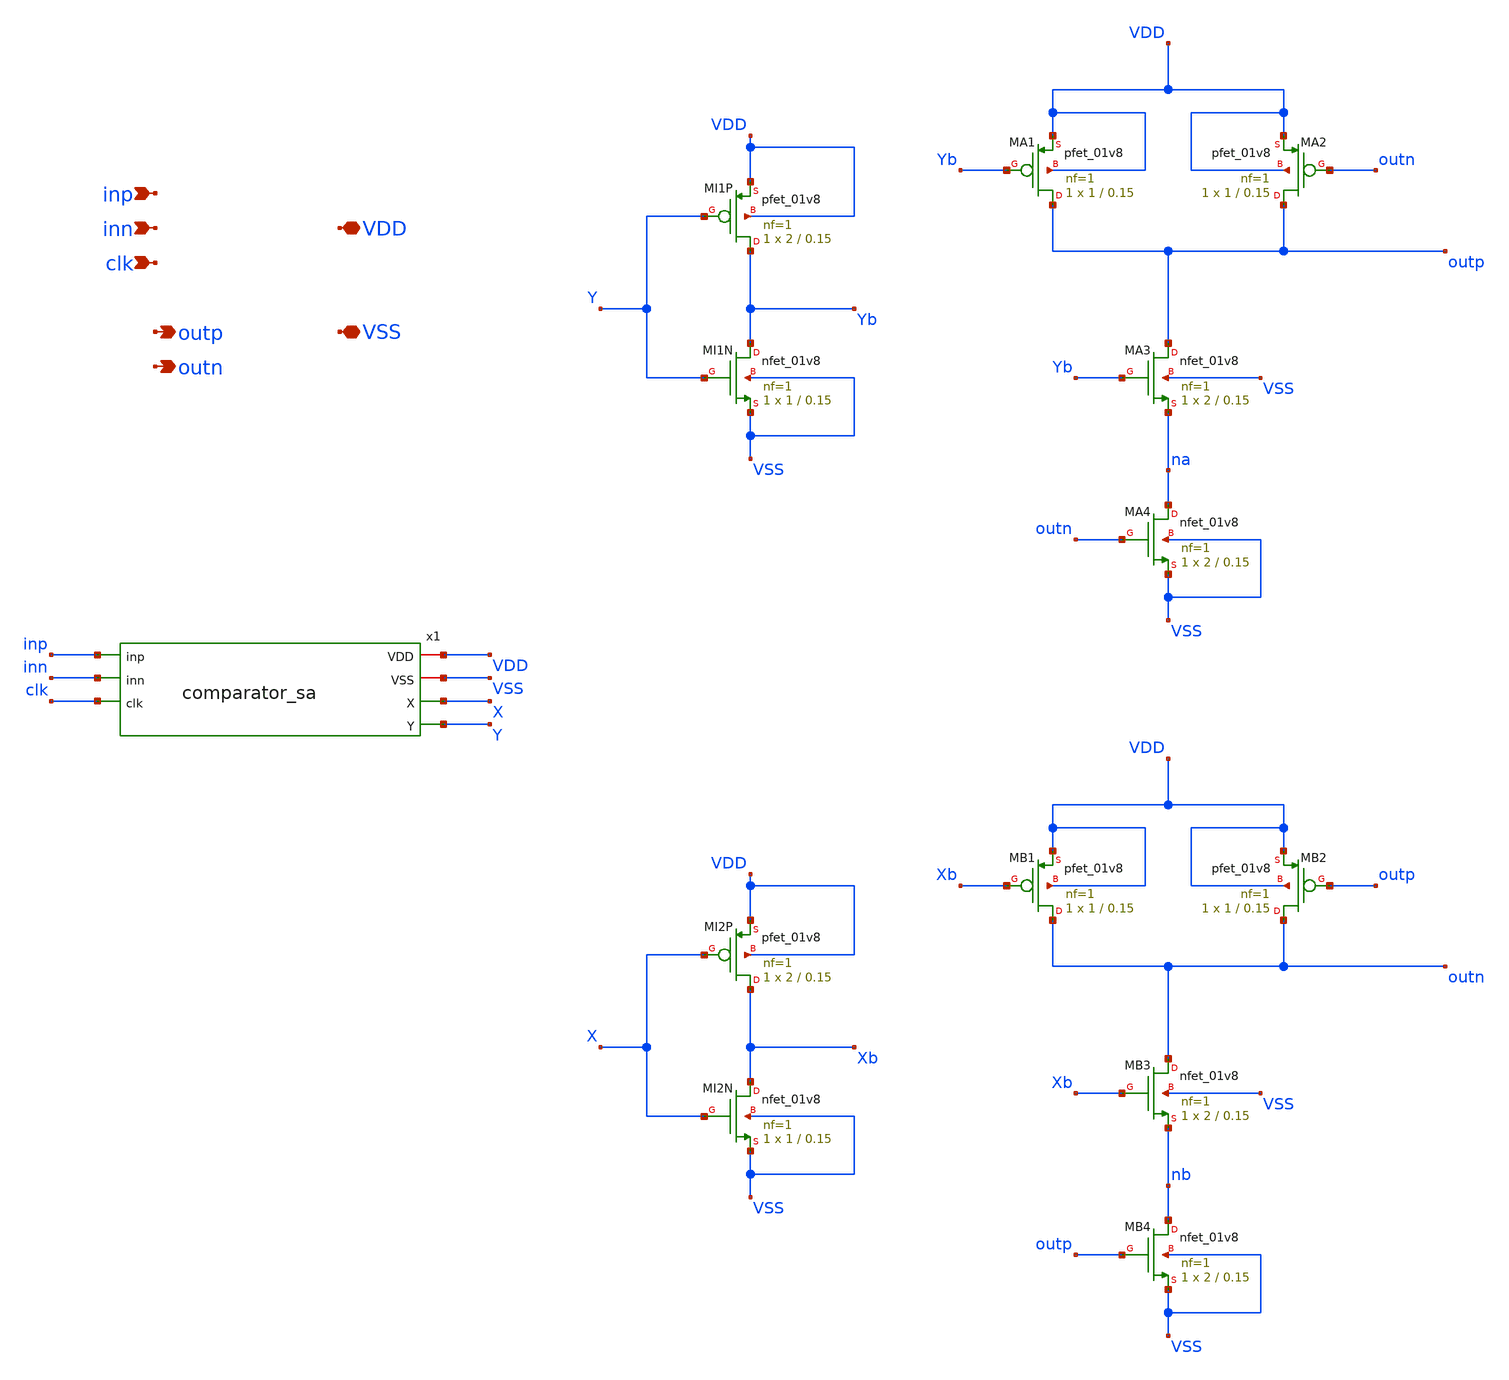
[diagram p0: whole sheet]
** sch_path: xschem/comparator.sch
**.subckt comparator inp inn clk outp outn VDD VSS
*.ipin inp
*.ipin inn
*.ipin clk
*.opin outp
*.opin outn
*.iopin VDD
*.iopin VSS
x1 inp VDD inn clk VSS X Y comparator_sa
XMI1N Yb Y VSS VSS sky130_fd_pr__nfet_01v8 L=0.15 W=1 nf=1 ad='int((1 + 1)/2) * 1 / 1 * 0.29' as='int((1 + 2)/2) * 1 / 1 * 0.29'
+ pd='2*int((1 + 1)/2) * (1 / 1 + 0.29)' ps='2*int((1 + 2)/2) * (1 / 1 + 0.29)' nrd='0.29 / 1 ' nrs='0.29 / 1 '
+ sa=0 sb=0 sd=0 mult=1 m=1
XMI1P Yb Y VDD VDD sky130_fd_pr__pfet_01v8 L=0.15 W=2 nf=1 ad='int((1 + 1)/2) * 2 / 1 * 0.29' as='int((1 + 2)/2) * 2 / 1 * 0.29'
+ pd='2*int((1 + 1)/2) * (2 / 1 + 0.29)' ps='2*int((1 + 2)/2) * (2 / 1 + 0.29)' nrd='0.29 / 2 ' nrs='0.29 / 2 '
+ sa=0 sb=0 sd=0 mult=1 m=1
XMI2N Xb X VSS VSS sky130_fd_pr__nfet_01v8 L=0.15 W=1 nf=1 ad='int((1 + 1)/2) * 1 / 1 * 0.29' as='int((1 + 2)/2) * 1 / 1 * 0.29'
+ pd='2*int((1 + 1)/2) * (1 / 1 + 0.29)' ps='2*int((1 + 2)/2) * (1 / 1 + 0.29)' nrd='0.29 / 1 ' nrs='0.29 / 1 '
+ sa=0 sb=0 sd=0 mult=1 m=1
XMI2P Xb X VDD VDD sky130_fd_pr__pfet_01v8 L=0.15 W=2 nf=1 ad='int((1 + 1)/2) * 2 / 1 * 0.29' as='int((1 + 2)/2) * 2 / 1 * 0.29'
+ pd='2*int((1 + 1)/2) * (2 / 1 + 0.29)' ps='2*int((1 + 2)/2) * (2 / 1 + 0.29)' nrd='0.29 / 2 ' nrs='0.29 / 2 '
+ sa=0 sb=0 sd=0 mult=1 m=1
XMA1 outp Yb VDD VDD sky130_fd_pr__pfet_01v8 L=0.15 W=1 nf=1 ad='int((1 + 1)/2) * 1 / 1 * 0.29' as='int((1 + 2)/2) * 1 / 1 * 0.29'
+ pd='2*int((1 + 1)/2) * (1 / 1 + 0.29)' ps='2*int((1 + 2)/2) * (1 / 1 + 0.29)' nrd='0.29 / 1 ' nrs='0.29 / 1 '
+ sa=0 sb=0 sd=0 mult=1 m=1
XMA2 outp outn VDD VDD sky130_fd_pr__pfet_01v8 L=0.15 W=1 nf=1 ad='int((1 + 1)/2) * 1 / 1 * 0.29' as='int((1 + 2)/2) * 1 / 1 * 0.29'
+ pd='2*int((1 + 1)/2) * (1 / 1 + 0.29)' ps='2*int((1 + 2)/2) * (1 / 1 + 0.29)' nrd='0.29 / 1 ' nrs='0.29 / 1 '
+ sa=0 sb=0 sd=0 mult=1 m=1
XMA3 outp Yb na VSS sky130_fd_pr__nfet_01v8 L=0.15 W=2 nf=1 ad='int((1 + 1)/2) * 2 / 1 * 0.29' as='int((1 + 2)/2) * 2 / 1 * 0.29'
+ pd='2*int((1 + 1)/2) * (2 / 1 + 0.29)' ps='2*int((1 + 2)/2) * (2 / 1 + 0.29)' nrd='0.29 / 2 ' nrs='0.29 / 2 '
+ sa=0 sb=0 sd=0 mult=1 m=1
XMA4 na outn VSS VSS sky130_fd_pr__nfet_01v8 L=0.15 W=2 nf=1 ad='int((1 + 1)/2) * 2 / 1 * 0.29' as='int((1 + 2)/2) * 2 / 1 * 0.29'
+ pd='2*int((1 + 1)/2) * (2 / 1 + 0.29)' ps='2*int((1 + 2)/2) * (2 / 1 + 0.29)' nrd='0.29 / 2 ' nrs='0.29 / 2 '
+ sa=0 sb=0 sd=0 mult=1 m=1
XMB1 outn Xb VDD VDD sky130_fd_pr__pfet_01v8 L=0.15 W=1 nf=1 ad='int((1 + 1)/2) * 1 / 1 * 0.29' as='int((1 + 2)/2) * 1 / 1 * 0.29'
+ pd='2*int((1 + 1)/2) * (1 / 1 + 0.29)' ps='2*int((1 + 2)/2) * (1 / 1 + 0.29)' nrd='0.29 / 1 ' nrs='0.29 / 1 '
+ sa=0 sb=0 sd=0 mult=1 m=1
XMB2 outn outp VDD VDD sky130_fd_pr__pfet_01v8 L=0.15 W=1 nf=1 ad='int((1 + 1)/2) * 1 / 1 * 0.29' as='int((1 + 2)/2) * 1 / 1 * 0.29'
+ pd='2*int((1 + 1)/2) * (1 / 1 + 0.29)' ps='2*int((1 + 2)/2) * (1 / 1 + 0.29)' nrd='0.29 / 1 ' nrs='0.29 / 1 '
+ sa=0 sb=0 sd=0 mult=1 m=1
XMB3 outn Xb nb VSS sky130_fd_pr__nfet_01v8 L=0.15 W=2 nf=1 ad='int((1 + 1)/2) * 2 / 1 * 0.29' as='int((1 + 2)/2) * 2 / 1 * 0.29'
+ pd='2*int((1 + 1)/2) * (2 / 1 + 0.29)' ps='2*int((1 + 2)/2) * (2 / 1 + 0.29)' nrd='0.29 / 2 ' nrs='0.29 / 2 '
+ sa=0 sb=0 sd=0 mult=1 m=1
XMB4 nb outp VSS VSS sky130_fd_pr__nfet_01v8 L=0.15 W=2 nf=1 ad='int((1 + 1)/2) * 2 / 1 * 0.29' as='int((1 + 2)/2) * 2 / 1 * 0.29'
+ pd='2*int((1 + 1)/2) * (2 / 1 + 0.29)' ps='2*int((1 + 2)/2) * (2 / 1 + 0.29)' nrd='0.29 / 2 ' nrs='0.29 / 2 '
+ sa=0 sb=0 sd=0 mult=1 m=1
**.ends

* expanding   symbol:  comparator_sa.sym # of pins=7
** sym_path: xschem/comparator_sa.sym
** sch_path: xschem/comparator_sa.sch
.subckt comparator_sa inp VDD inn clk VSS X Y
*.ipin inp
*.ipin inn
*.ipin clk
*.opin X
*.opin Y
*.iopin VDD
*.iopin VSS
XM7 T ckb VDD VDD sky130_fd_pr__pfet_01v8 L=0.15 W=4 nf=1 ad='int((1 + 1)/2) * 4 / 1 * 0.29' as='int((1 + 2)/2) * 4 / 1 * 0.29'
+ pd='2*int((1 + 1)/2) * (4 / 1 + 0.29)' ps='2*int((1 + 2)/2) * (4 / 1 + 0.29)' nrd='0.29 / 4 ' nrs='0.29 / 4 '
+ sa=0 sb=0 sd=0 mult=1 m=1
XM1 P inp T T sky130_fd_pr__pfet_01v8 L=0.5 W=8 nf=4 ad='int((4 + 1)/2) * 8 / 4 * 0.29' as='int((4 + 2)/2) * 8 / 4 * 0.29'
+ pd='2*int((4 + 1)/2) * (8 / 4 + 0.29)' ps='2*int((4 + 2)/2) * (8 / 4 + 0.29)' nrd='0.29 / 8 ' nrs='0.29 / 8 '
+ sa=0 sb=0 sd=0 mult=1 m=1
XM2 Q inn T T sky130_fd_pr__pfet_01v8 L=0.5 W=8 nf=4 ad='int((4 + 1)/2) * 8 / 4 * 0.29' as='int((4 + 2)/2) * 8 / 4 * 0.29'
+ pd='2*int((4 + 1)/2) * (8 / 4 + 0.29)' ps='2*int((4 + 2)/2) * (8 / 4 + 0.29)' nrd='0.29 / 8 ' nrs='0.29 / 8 '
+ sa=0 sb=0 sd=0 mult=1 m=1
XM3 X Y P VDD sky130_fd_pr__pfet_01v8 L=0.15 W=2 nf=1 ad='int((1 + 1)/2) * 2 / 1 * 0.29' as='int((1 + 2)/2) * 2 / 1 * 0.29'
+ pd='2*int((1 + 1)/2) * (2 / 1 + 0.29)' ps='2*int((1 + 2)/2) * (2 / 1 + 0.29)' nrd='0.29 / 2 ' nrs='0.29 / 2 '
+ sa=0 sb=0 sd=0 mult=1 m=1
XM4 Y X Q VDD sky130_fd_pr__pfet_01v8 L=0.15 W=2 nf=1 ad='int((1 + 1)/2) * 2 / 1 * 0.29' as='int((1 + 2)/2) * 2 / 1 * 0.29'
+ pd='2*int((1 + 1)/2) * (2 / 1 + 0.29)' ps='2*int((1 + 2)/2) * (2 / 1 + 0.29)' nrd='0.29 / 2 ' nrs='0.29 / 2 '
+ sa=0 sb=0 sd=0 mult=1 m=1
XM6 Y X VSS VSS sky130_fd_pr__nfet_01v8 L=0.15 W=1 nf=1 ad='int((1 + 1)/2) * 1 / 1 * 0.29' as='int((1 + 2)/2) * 1 / 1 * 0.29'
+ pd='2*int((1 + 1)/2) * (1 / 1 + 0.29)' ps='2*int((1 + 2)/2) * (1 / 1 + 0.29)' nrd='0.29 / 1 ' nrs='0.29 / 1 '
+ sa=0 sb=0 sd=0 mult=1 m=1
XM5 X Y VSS VSS sky130_fd_pr__nfet_01v8 L=0.15 W=1 nf=1 ad='int((1 + 1)/2) * 1 / 1 * 0.29' as='int((1 + 2)/2) * 1 / 1 * 0.29'
+ pd='2*int((1 + 1)/2) * (1 / 1 + 0.29)' ps='2*int((1 + 2)/2) * (1 / 1 + 0.29)' nrd='0.29 / 1 ' nrs='0.29 / 1 '
+ sa=0 sb=0 sd=0 mult=1 m=1
XS4 Y ckb VSS VSS sky130_fd_pr__nfet_01v8 L=0.6 W=2 nf=1 ad='int((1 + 1)/2) * 2 / 1 * 0.29' as='int((1 + 2)/2) * 2 / 1 * 0.29'
+ pd='2*int((1 + 1)/2) * (2 / 1 + 0.29)' ps='2*int((1 + 2)/2) * (2 / 1 + 0.29)' nrd='0.29 / 2 ' nrs='0.29 / 2 '
+ sa=0 sb=0 sd=0 mult=1 m=1
XS2 Q ckb VSS VSS sky130_fd_pr__nfet_01v8 L=0.6 W=2 nf=1 ad='int((1 + 1)/2) * 2 / 1 * 0.29' as='int((1 + 2)/2) * 2 / 1 * 0.29'
+ pd='2*int((1 + 1)/2) * (2 / 1 + 0.29)' ps='2*int((1 + 2)/2) * (2 / 1 + 0.29)' nrd='0.29 / 2 ' nrs='0.29 / 2 '
+ sa=0 sb=0 sd=0 mult=1 m=1
XS3 X ckb VSS VSS sky130_fd_pr__nfet_01v8 L=0.6 W=2 nf=1 ad='int((1 + 1)/2) * 2 / 1 * 0.29' as='int((1 + 2)/2) * 2 / 1 * 0.29'
+ pd='2*int((1 + 1)/2) * (2 / 1 + 0.29)' ps='2*int((1 + 2)/2) * (2 / 1 + 0.29)' nrd='0.29 / 2 ' nrs='0.29 / 2 '
+ sa=0 sb=0 sd=0 mult=1 m=1
XS1 P ckb VSS VSS sky130_fd_pr__nfet_01v8 L=0.6 W=2 nf=1 ad='int((1 + 1)/2) * 2 / 1 * 0.29' as='int((1 + 2)/2) * 2 / 1 * 0.29'
+ pd='2*int((1 + 1)/2) * (2 / 1 + 0.29)' ps='2*int((1 + 2)/2) * (2 / 1 + 0.29)' nrd='0.29 / 2 ' nrs='0.29 / 2 '
+ sa=0 sb=0 sd=0 mult=1 m=1
XMIN ckb clk VSS VSS sky130_fd_pr__nfet_01v8 L=0.15 W=1 nf=1 ad='int((1 + 1)/2) * 1 / 1 * 0.29' as='int((1 + 2)/2) * 1 / 1 * 0.29'
+ pd='2*int((1 + 1)/2) * (1 / 1 + 0.29)' ps='2*int((1 + 2)/2) * (1 / 1 + 0.29)' nrd='0.29 / 1 ' nrs='0.29 / 1 '
+ sa=0 sb=0 sd=0 mult=1 m=1
XMIP ckb clk VDD VDD sky130_fd_pr__pfet_01v8 L=0.15 W=2 nf=1 ad='int((1 + 1)/2) * 2 / 1 * 0.29' as='int((1 + 2)/2) * 2 / 1 * 0.29'
+ pd='2*int((1 + 1)/2) * (2 / 1 + 0.29)' ps='2*int((1 + 2)/2) * (2 / 1 + 0.29)' nrd='0.29 / 2 ' nrs='0.29 / 2 '
+ sa=0 sb=0 sd=0 mult=1 m=1
.ends

.end
